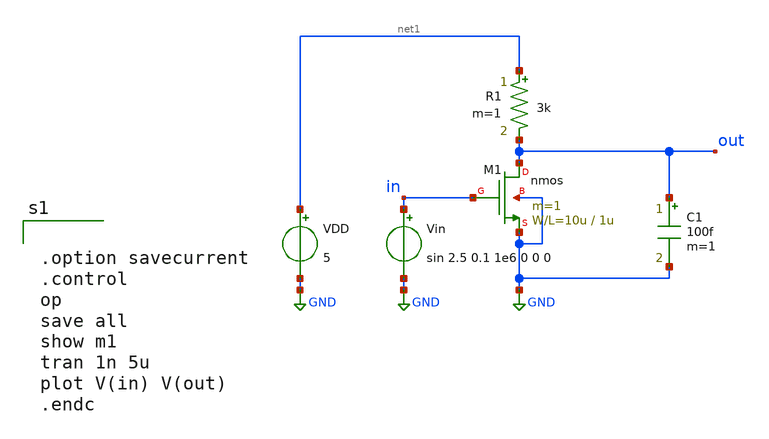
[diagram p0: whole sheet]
** sch_path: member_project/GroupWork/Team_masahiro/nfet_common_source_tran.sch
**.subckt nfet_common_source_tran
M1 out in GND GND nmos L=1u W=10u m=1
R1 net1 out 3k m=1
VDD net1 GND 5
Vin in GND sin 2.5 0.1 1e6 0 0 0
C1 out GND 100f m=1
**** begin user architecture code
 .include $::LIB/mos.lib
.include $::LIB/passive.lib
.include $::LIB/diode.lib


.option savecurrent
.control
op
save all
show m1
tran 1n 5u
plot V(in) V(out)
.endc


**** end user architecture code
**.ends
.GLOBAL GND
.end
